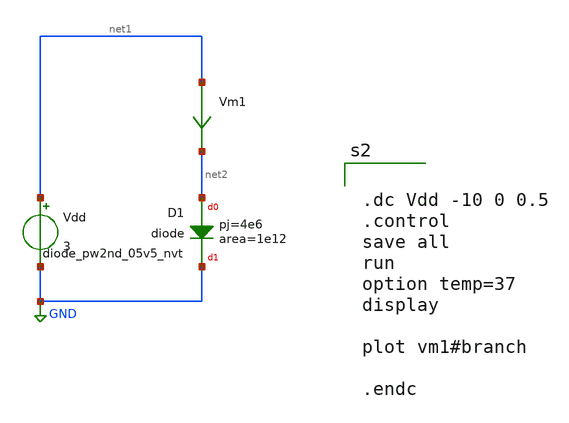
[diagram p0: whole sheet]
** sch_path: xschem/cmos_imager/tb_diode_vi.sch
**.subckt tb_diode_vi
XD1 net2 GND sky130_fd_pr__diode_pw2nd_05v5_nvt area=1e12 pj=4e6
Vdd net1 GND 3
Vm1 net1 net2 0
.save i(vm1)
**** begin user architecture code


.dc Vdd -10 0 0.5
.control
save all
run
option temp=37
display

plot vm1#branch

.endc



** opencircuitdesign pdks install
.lib $::SKYWATER_MODELS/sky130.lib.spice tt


**** end user architecture code
**.ends
.GLOBAL GND
.end
